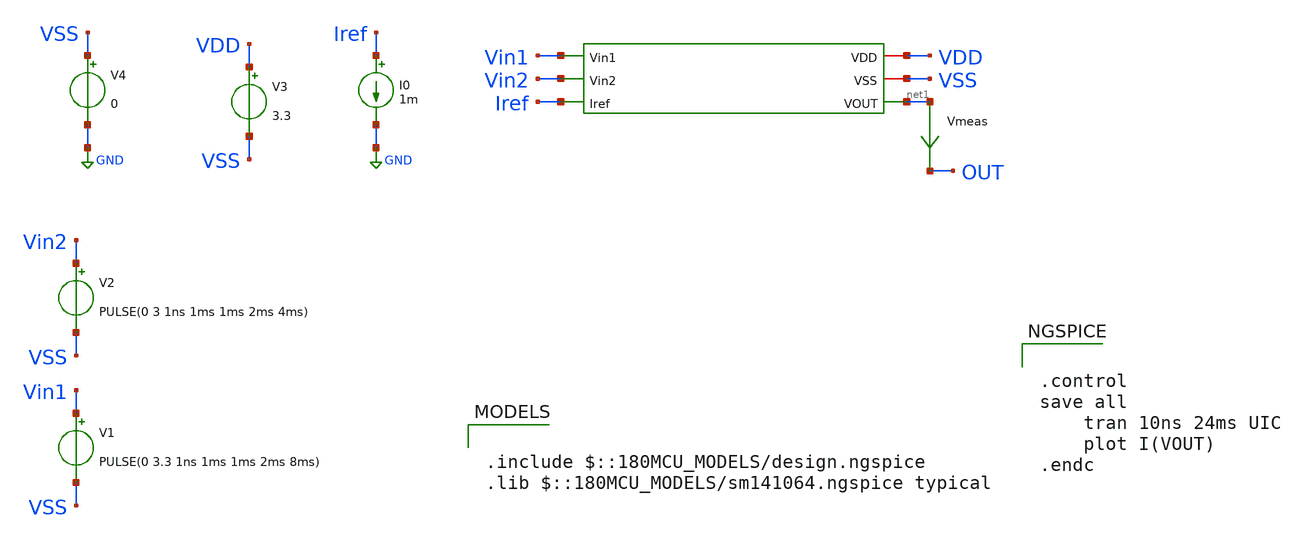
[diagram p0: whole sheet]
** sch_path: week02_current_diffpair/tugas5_cascode_current_mirror/nmos-ota-testbench.sch
**.subckt nmos-ota-testbench
I0 Iref GND 1m
V1 Vin1 VSS PULSE(0 3.3 1ns 1ms 1ms 2ms 8ms)
V2 Vin2 VSS PULSE(0 3 1ns 1ms 1ms 2ms 4ms)
V3 VDD VSS 3.3
V4 VSS GND 0
Vmeas net1 OUT 0
.save i(vmeas)
**** begin user architecture code

.include $::180MCU_MODELS/design.ngspice
.lib $::180MCU_MODELS/sm141064.ngspice typical



.control
save all
	tran 10ns 24ms UIC
	plot I(VOUT)
.endc


**** end user architecture code
**.ends
.GLOBAL GND
.end
